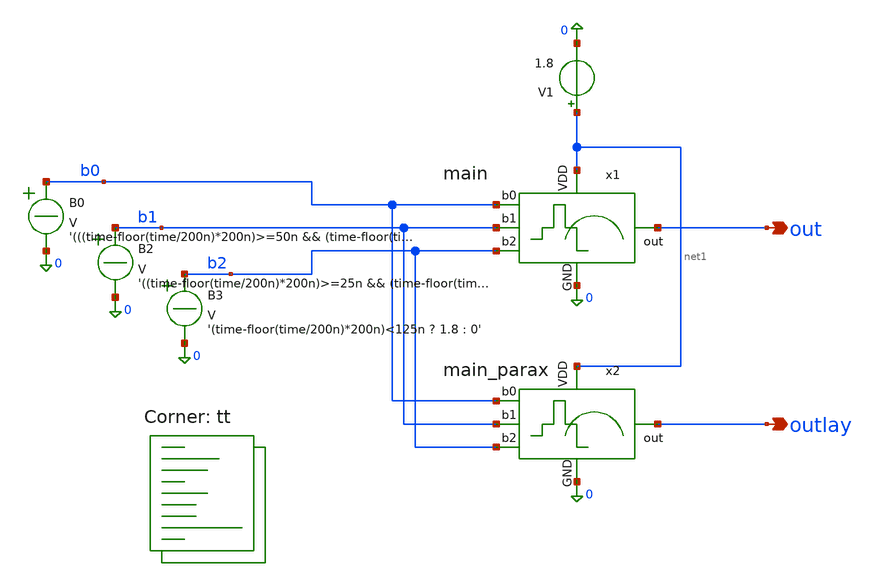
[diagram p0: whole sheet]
** sch_path: xschem/main_tb_postlayout.sch
**.subckt main_tb_postlayout out outlay
*.opin out
*.opin outlay
B0 b0 0 V = '(((time-floor(time/200n)*200n)>=50n && (time-floor(time/200n)*200n)<75n) || ((time-floor(time/200n)*200n)>=125n && (time-floor(time/200n)*200n)<150n) || ((time-floor(time/200n)*200n)>=175n && (time-floor(time/200n)*200n)<200n)) ? 1.8 : 0'
B2 b1 0 V = '((time-floor(time/200n)*200n)>=25n && (time-floor(time/200n)*200n)<100n) ? 1.8 : 0'
B3 b2 0 V = '(time-floor(time/200n)*200n)<125n ? 1.8 : 0'
V1 net1 0 1.8
x1 net1 b0 out b1 b2 0 main
x2 net1 b0 outlay b1 b2 0 main_parax
**** begin user architecture code
.lib $::SKYWATER_MODELS/sky130.lib.spice tt


.control
save all
.param f=5Meg
.param Fs=20Meg
.param Ts={1/Fs}
tran 1n 60000n
write main_postlayout_tran.raw
op
write main_postlayout_op.raw
ac dec 20 1 100meg
write main_postlayout_ac.raw
.endc

**** end user architecture code
**.ends

* expanding   symbol:  main.sym # of pins=6
** sym_path: xschem/main.sym
** sch_path: xschem/main.sch
.subckt main VDD b0 out b1 b2 GND
*.ipin VDD
*.ipin GND
*.ipin b0
*.ipin b1
*.ipin b2
*.opin out
x5 b0 b1 b2 VDD v_dac GND DAC3bit
x1 VDD v_dac out GND otaSys_5t_sky130
.ends


* expanding   symbol:  main_parax.sym # of pins=6
** sym_path: xschem/main.sym
.include [file normalize ../mag/main.sim.spice]

* expanding   symbol:  DAC3bit.sym # of pins=6
** sym_path: xschem/DAC3bit.sym
** sch_path: xschem/DAC3bit.sch
.subckt DAC3bit b0 b1 b2 VDD out GND
*.opin out
*.ipin b0
*.ipin b1
*.ipin b2
*.ipin GND
*.ipin VDD
XR1 GND net3 sky130_fd_pr__res_generic_po W=1 L=21 m=1
XR2 net3 net1 sky130_fd_pr__res_generic_po W=1 L=21 m=1
XR3 b0 net4 sky130_fd_pr__res_generic_po W=1 L=21 m=1
XR4 net4 net1 sky130_fd_pr__res_generic_po W=1 L=21 m=1
XR5 b1 net5 sky130_fd_pr__res_generic_po W=1 L=21 m=1
XR6 net5 net2 sky130_fd_pr__res_generic_po W=1 L=21 m=1
XR7 b2 net6 sky130_fd_pr__res_generic_po W=1 L=21 m=1
XR8 net6 vx sky130_fd_pr__res_generic_po W=1 L=21 m=1
XR9 net1 net2 sky130_fd_pr__res_generic_po W=1 L=21 m=1
XR10 net2 vx sky130_fd_pr__res_generic_po W=1 L=21 m=1
XR12 VDD out sky130_fd_pr__res_generic_po W=1 L=21 m=1
XR13 out GND sky130_fd_pr__res_generic_po W=1 L=21 m=1
XR11 out vx sky130_fd_pr__res_generic_po W=1 L=63 m=1
.ends


* expanding   symbol:  otaSys_5t_sky130.sym # of pins=4
** sym_path: xschem/otaSys_5t_sky130.sym
** sch_path: xschem/otaSys_5t_sky130.sch
.subckt otaSys_5t_sky130 VDD in out GND
*.opin out
*.ipin in
*.ipin GND
*.ipin VDD
x1 VDD net1 net2 in GND ota_5t_sky130
x2 VDD out net1 net2 GND ota_5t_sky130
x3 VDD net1 net2 out GND ota_5t_sky130
x4 VDD out out net2 GND otaq_5t_sky130
XC1 net1 GND sky130_fd_pr__cap_mim_m3_1 W=30 L=30 MF=4 m=4
XC2 out GND sky130_fd_pr__cap_mim_m3_1 W=30 L=30 MF=4 m=4
XR1 VDD net2 GND sky130_fd_pr__res_high_po_1p41 L=88.83 mult=1 m=1
XR2 net2 GND GND sky130_fd_pr__res_high_po_1p41 L=88.83 mult=1 m=1
.ends


* expanding   symbol:  ota_5t_sky130.sym # of pins=5
** sym_path: xschem/ota_5t_sky130.sym
** sch_path: xschem/ota_5t_sky130.sch
.subckt ota_5t_sky130 VDD VOUT VINP VINN GND
*.ipin VINP
*.ipin VINN
*.opin VOUT
*.ipin VDD
*.ipin GND
XM5 V5 VDD GND GND sky130_fd_pr__nfet_01v8 L=1.475 W=4 nf=1 ad='int((1 + 1)/2) * 4 / 1 * 0.29' as='int((1 + 2)/2) * 4 / 1 * 0.29'
+ pd='2*int((1 + 1)/2) * (4 / 1 + 0.29)' ps='2*int((1 + 2)/2) * (4 / 1 + 0.29)' nrd='0.29 / 4 ' nrs='0.29 / 4 '
+ sa=0 sb=0 sd=0 mult=1 m=1
XM1 net1 VINP V5 GND sky130_fd_pr__nfet_01v8 L=0.5 W=2 nf=1 ad='int((1 + 1)/2) * 2 / 1 * 0.29' as='int((1 + 2)/2) * 2 / 1 * 0.29'
+ pd='2*int((1 + 1)/2) * (2 / 1 + 0.29)' ps='2*int((1 + 2)/2) * (2 / 1 + 0.29)' nrd='0.29 / 2 ' nrs='0.29 / 2 '
+ sa=0 sb=0 sd=0 mult=1 m=1
XM2 VOUT VINN V5 GND sky130_fd_pr__nfet_01v8 L=0.5 W=2 nf=1 ad='int((1 + 1)/2) * 2 / 1 * 0.29' as='int((1 + 2)/2) * 2 / 1 * 0.29'
+ pd='2*int((1 + 1)/2) * (2 / 1 + 0.29)' ps='2*int((1 + 2)/2) * (2 / 1 + 0.29)' nrd='0.29 / 2 ' nrs='0.29 / 2 '
+ sa=0 sb=0 sd=0 mult=1 m=1
XM3 net1 net1 VDD VDD sky130_fd_pr__pfet_01v8 L=0.5 W=5 nf=1 ad='int((1 + 1)/2) * 5 / 1 * 0.29' as='int((1 + 2)/2) * 5 / 1 * 0.29'
+ pd='2*int((1 + 1)/2) * (5 / 1 + 0.29)' ps='2*int((1 + 2)/2) * (5 / 1 + 0.29)' nrd='0.29 / 5 ' nrs='0.29 / 5 '
+ sa=0 sb=0 sd=0 mult=1 m=1
XM4 VOUT net1 VDD VDD sky130_fd_pr__pfet_01v8 L=0.5 W=5 nf=1 ad='int((1 + 1)/2) * 5 / 1 * 0.29' as='int((1 + 2)/2) * 5 / 1 * 0.29'
+ pd='2*int((1 + 1)/2) * (5 / 1 + 0.29)' ps='2*int((1 + 2)/2) * (5 / 1 + 0.29)' nrd='0.29 / 5 ' nrs='0.29 / 5 '
+ sa=0 sb=0 sd=0 mult=1 m=1
XM6 VDD VDD GND GND sky130_fd_pr__nfet_01v8 L=0.5 W=4 nf=1 ad='int((1 + 1)/2) * 4 / 1 * 0.29' as='int((1 + 2)/2) * 4 / 1 * 0.29'
+ pd='2*int((1 + 1)/2) * (4 / 1 + 0.29)' ps='2*int((1 + 2)/2) * (4 / 1 + 0.29)' nrd='0.29 / 4 ' nrs='0.29 / 4 '
+ sa=0 sb=0 sd=0 mult=1 m=1
.ends


* expanding   symbol:  otaq_5t_sky130.sym # of pins=5
** sym_path: xschem/otaq_5t_sky130.sym
** sch_path: xschem/otaq_5t_sky130.sch
.subckt otaq_5t_sky130 VDD VOUT VINP VINN GND
*.ipin VINP
*.ipin VINN
*.opin VOUT
*.ipin VDD
*.ipin GND
XM5 net2 VDD GND GND sky130_fd_pr__nfet_01v8 L=20 W=0.5 nf=1 ad='int((1 + 1)/2) * 0.5 / 1 * 0.29' as='int((1 + 2)/2) * 0.5 / 1 * 0.29'
+ pd='2*int((1 + 1)/2) * (0.5 / 1 + 0.29)' ps='2*int((1 + 2)/2) * (0.5 / 1 + 0.29)' nrd='0.29 / 0.5 ' nrs='0.29 / 0.5 '
+ sa=0 sb=0 sd=0 mult=1 m=1
XM1 net1 VINP net2 GND sky130_fd_pr__nfet_01v8 L=7 W=0.5 nf=1 ad='int((1 + 1)/2) * 0.5 / 1 * 0.29' as='int((1 + 2)/2) * 0.5 / 1 * 0.29'
+ pd='2*int((1 + 1)/2) * (0.5 / 1 + 0.29)' ps='2*int((1 + 2)/2) * (0.5 / 1 + 0.29)' nrd='0.29 / 0.5 ' nrs='0.29 / 0.5 '
+ sa=0 sb=0 sd=0 mult=1 m=1
XM2 VOUT VINN net2 GND sky130_fd_pr__nfet_01v8 L=7 W=0.5 nf=1 ad='int((1 + 1)/2) * 0.5 / 1 * 0.29' as='int((1 + 2)/2) * 0.5 / 1 * 0.29'
+ pd='2*int((1 + 1)/2) * (0.5 / 1 + 0.29)' ps='2*int((1 + 2)/2) * (0.5 / 1 + 0.29)' nrd='0.29 / 0.5 ' nrs='0.29 / 0.5 '
+ sa=0 sb=0 sd=0 mult=1 m=1
XM3 net1 net1 VDD VDD sky130_fd_pr__pfet_01v8 L=7 W=1 nf=1 ad='int((1 + 1)/2) * 1 / 1 * 0.29' as='int((1 + 2)/2) * 1 / 1 * 0.29'
+ pd='2*int((1 + 1)/2) * (1 / 1 + 0.29)' ps='2*int((1 + 2)/2) * (1 / 1 + 0.29)' nrd='0.29 / 1 ' nrs='0.29 / 1 '
+ sa=0 sb=0 sd=0 mult=1 m=1
XM4 VOUT net1 VDD VDD sky130_fd_pr__pfet_01v8 L=7 W=1 nf=1 ad='int((1 + 1)/2) * 1 / 1 * 0.29' as='int((1 + 2)/2) * 1 / 1 * 0.29'
+ pd='2*int((1 + 1)/2) * (1 / 1 + 0.29)' ps='2*int((1 + 2)/2) * (1 / 1 + 0.29)' nrd='0.29 / 1 ' nrs='0.29 / 1 '
+ sa=0 sb=0 sd=0 mult=1 m=1
XM6 VDD VDD GND GND sky130_fd_pr__nfet_01v8 L=0.5 W=1 nf=1 ad='int((1 + 1)/2) * 1 / 1 * 0.29' as='int((1 + 2)/2) * 1 / 1 * 0.29'
+ pd='2*int((1 + 1)/2) * (1 / 1 + 0.29)' ps='2*int((1 + 2)/2) * (1 / 1 + 0.29)' nrd='0.29 / 1 ' nrs='0.29 / 1 '
+ sa=0 sb=0 sd=0 mult=1 m=1
.ends

.end
